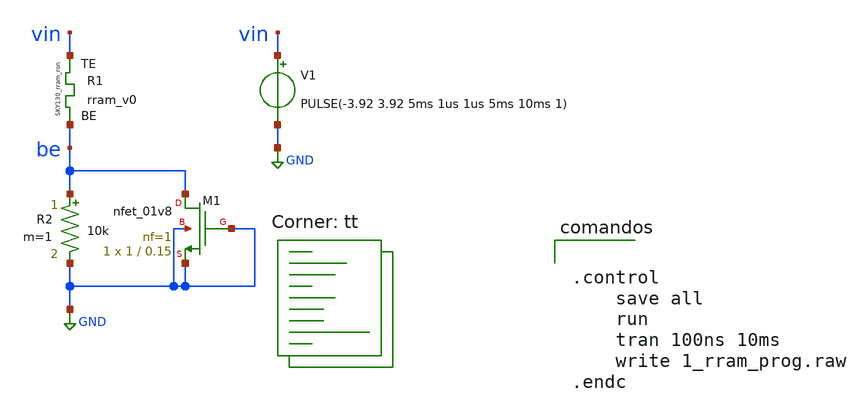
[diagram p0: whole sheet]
** sch_path: rram_programming/1_rram_prog.sch
**.subckt 1_rram_prog
V1 vin GND PULSE(-3.92 3.92 5ms 1us 1us 5ms 10ms 1)
XM1 be GND GND GND sky130_fd_pr__nfet_01v8 L=0.15 W=1 nf=1 ad='int((nf+1)/2) * W/nf * 0.29' as='int((nf+2)/2) * W/nf * 0.29'
+ pd='2*int((nf+1)/2) * (W/nf + 0.29)' ps='2*int((nf+2)/2) * (W/nf + 0.29)' nrd='0.29 / W' nrs='0.29 / W'
+ sa=0 sb=0 sd=0 mult=1 m=1
XR1 vin be rram_v0
R2 be GND 10k m=1
**** begin user architecture code
.lib $::SKYWATER_MODELS/sky130.lib.spice tt

** opencircuitdesign pdks install
.inc $::SKYWATER_MODELS/rram_v0.spice



.control
	save all
	run
	tran 100ns 10ms
	write 1_rram_prog.raw
.endc



**** end user architecture code
**.ends
.GLOBAL GND
.end
